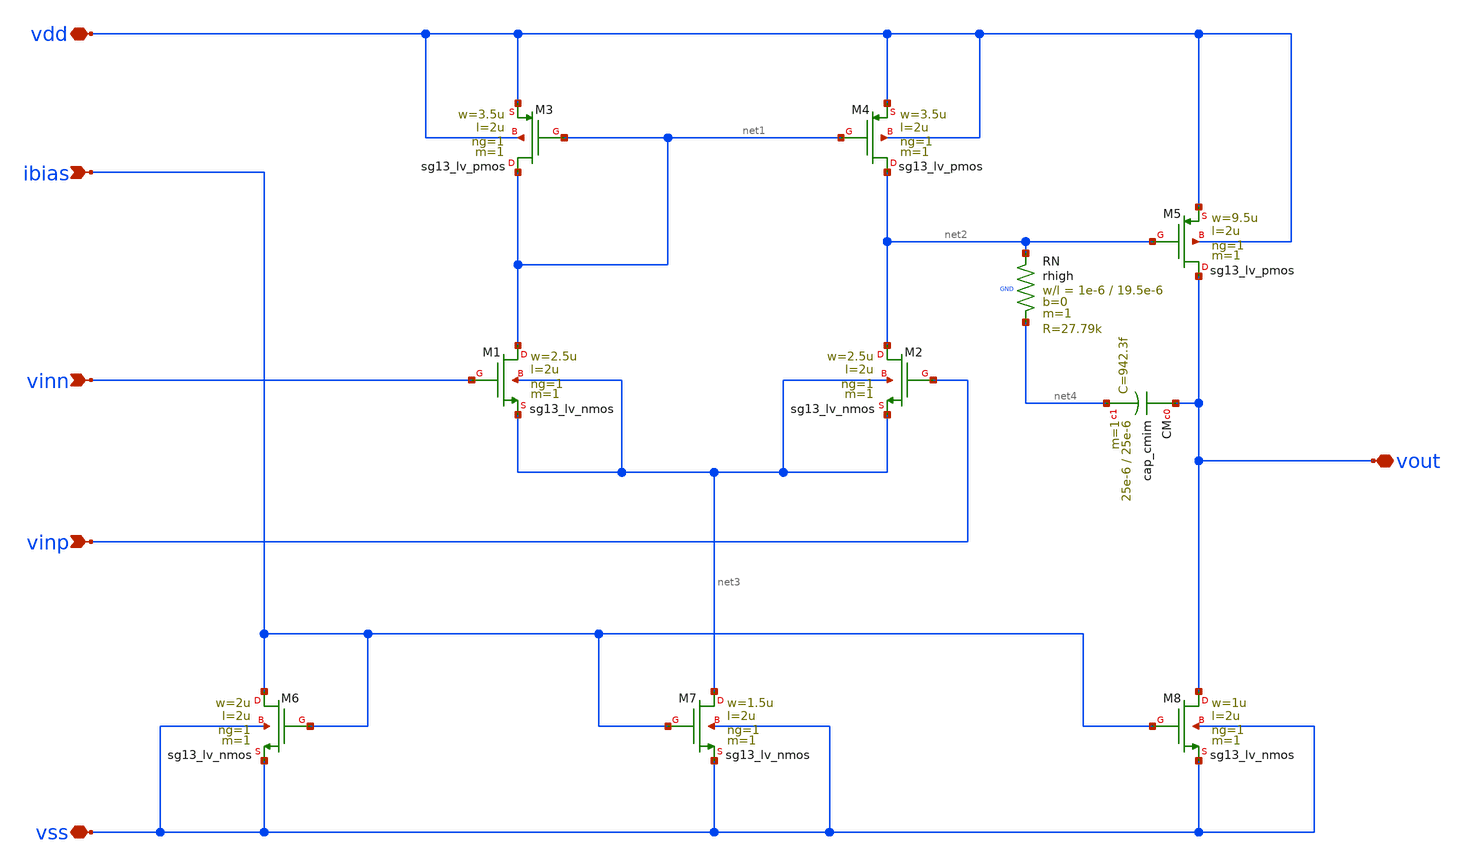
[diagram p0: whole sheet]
** sch_path: xschem/lpf-ota-2stage.sch
**.subckt lpf-ota-2stage vdd vss ibias vout vinn vinp
*.iopin vdd
*.iopin vss
*.ipin ibias
*.iopin vout
*.ipin vinn
*.ipin vinp
XM1 net1 vinn net3 net3 sg13_lv_nmos w=2.5u l=2u ng=1 m=1 mm_ok=1
XM2 net2 vinp net3 net3 sg13_lv_nmos w=2.5u l=2u ng=1 m=1 mm_ok=1
XM4 net2 net1 vdd vdd sg13_lv_pmos w=3.5u l=2u ng=1 m=1 mm_ok=1
XM3 net1 net1 vdd vdd sg13_lv_pmos w=3.5u l=2u ng=1 m=1 mm_ok=1
XM5 vout net2 vdd vdd sg13_lv_pmos w=9.5u l=2u ng=1 m=1 mm_ok=1
XM6 ibias ibias vss vss sg13_lv_nmos w=2u l=2u ng=1 m=1 mm_ok=1
XM7 net3 ibias vss vss sg13_lv_nmos w=1.5u l=2u ng=1 m=1 mm_ok=1
XM8 vout ibias vss vss sg13_lv_nmos w=1u l=2u ng=1 m=1 mm_ok=1
XCM vout net4 cap_cmim w=25e-6 l=25e-6 m=1 mm_ok=1
XRN net2 net4 GND rhigh w=1e-6 l=19.5e-6 m=1 b=0 mm_ok=1
**.ends
.end
